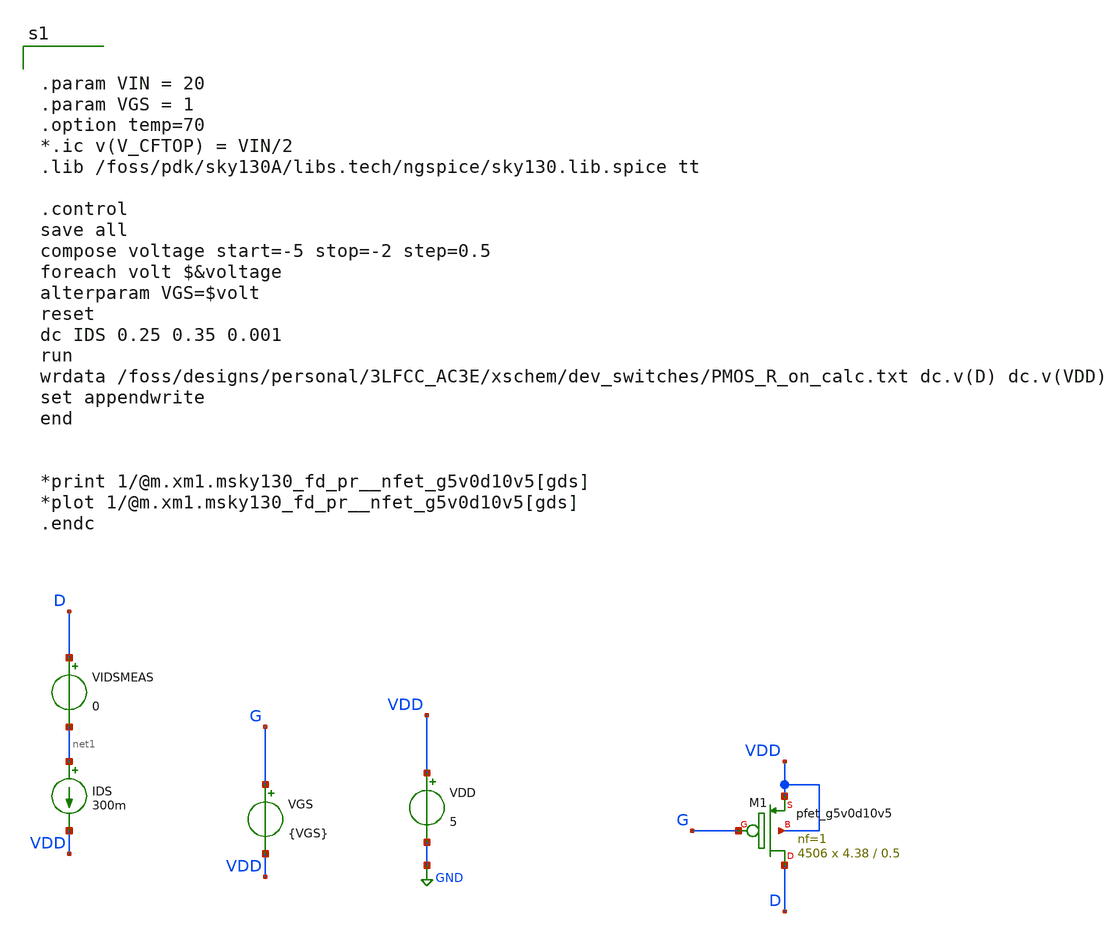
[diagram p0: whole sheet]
** sch_path: Notebooks/3LFCC/PMOS_allfingers_RONcalc.sch
**.subckt PMOS_allfingers_RONcalc
VGS G VDD {VGS}
IDS net1 VDD 300m
VIDSMEAS D net1 0
XM1 D G VDD VDD sky130_fd_pr__pfet_g5v0d10v5 L=0.5 W=4.38 nf=1 ad='int((nf+1)/2) * W/nf * 0.29' as='int((nf+2)/2) * W/nf * 0.29'
+ pd='2*int((nf+1)/2) * (W/nf + 0.29)' ps='2*int((nf+2)/2) * (W/nf + 0.29)' nrd='0.29 / W' nrs='0.29 / W'
+ sa=0 sb=0 sd=0 mult=4506 m=4506
VDD VDD GND 5
**** begin user architecture code


.param VIN = 20
.param VGS = 1
.option temp=70
*.ic v(V_CFTOP) = VIN/2
.lib /foss/pdk/sky130A/libs.tech/ngspice/sky130.lib.spice tt

.control
save all
compose voltage start=-5 stop=-2 step=0.5
foreach volt $&voltage
alterparam VGS=$volt
reset
dc IDS 0.25 0.35 0.001
run
wrdata /foss/designs/personal/3LFCC_AC3E/xschem/dev_switches/PMOS_R_on_calc.txt dc.v(D) dc.v(VDD)
set appendwrite
end


*print 1/@m.xm1.msky130_fd_pr__nfet_g5v0d10v5[gds]
*plot 1/@m.xm1.msky130_fd_pr__nfet_g5v0d10v5[gds]
.endc



**** end user architecture code
**.ends
.GLOBAL GND
.end
